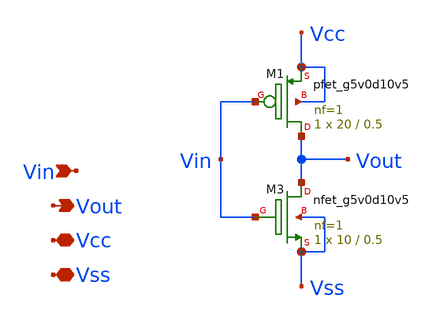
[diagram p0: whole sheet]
** sch_path: Git Files/Simulation Schematic/Inverter netlists/inv_0_5_3v3.sch
**.subckt inv_0_5_3v3 Vin Vout Vcc Vss
*.ipin Vin
*.opin Vout
*.iopin Vcc
*.iopin Vss
XM3 Vout Vin Vss Vss sky130_fd_pr__nfet_g5v0d10v5 L=0.5 W=10 nf=1 ad='int((nf+1)/2) * W/nf * 0.29' as='int((nf+2)/2) * W/nf * 0.29'
+ pd='2*int((nf+1)/2) * (W/nf + 0.29)' ps='2*int((nf+2)/2) * (W/nf + 0.29)' nrd='0.29 / W' nrs='0.29 / W'
+ sa=0 sb=0 sd=0 mult=1 m=1
XM1 Vout Vin Vcc Vcc sky130_fd_pr__pfet_g5v0d10v5 L=0.5 W=20 nf=1 ad='int((nf+1)/2) * W/nf * 0.29' as='int((nf+2)/2) * W/nf * 0.29'
+ pd='2*int((nf+1)/2) * (W/nf + 0.29)' ps='2*int((nf+2)/2) * (W/nf + 0.29)' nrd='0.29 / W' nrs='0.29 / W'
+ sa=0 sb=0 sd=0 mult=1 m=1
**.ends
.end
